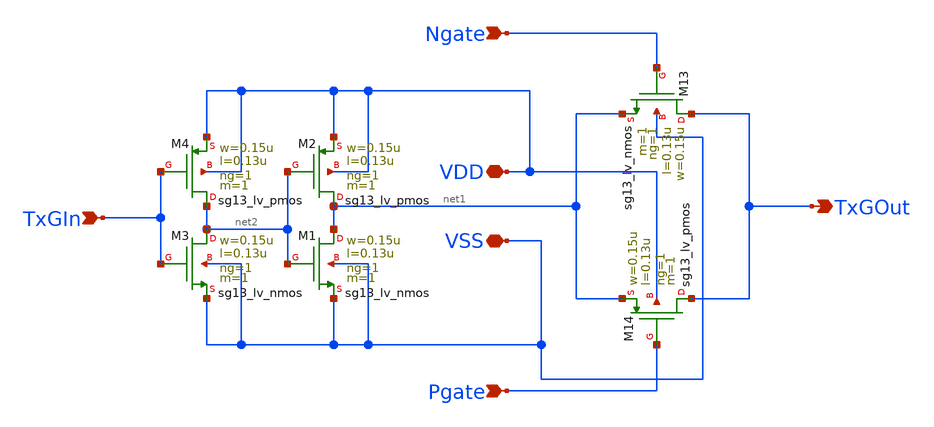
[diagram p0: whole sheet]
** sch_path: circuit_files/xschem_symbols/TxGate.sch
**.subckt TxGate Ngate Pgate TxGIn TxGOut VDD VSS
*.ipin Ngate
*.ipin Pgate
*.ipin TxGIn
*.opin TxGOut
*.iopin VDD
*.iopin VSS
XM13 TxGOut Ngate net1 VSS sg13_lv_nmos w=0.15u l=0.13u ng=1 m=1 mm_ok=1
XM14 TxGOut Pgate net1 VDD sg13_lv_pmos w=0.15u l=0.13u ng=1 m=1 mm_ok=1
XM1 net1 net2 VSS VSS sg13_lv_nmos w=0.15u l=0.13u ng=1 m=1 mm_ok=1
XM2 net1 net2 VDD VDD sg13_lv_pmos w=0.15u l=0.13u ng=1 m=1 mm_ok=1
XM3 net2 TxGIn VSS VSS sg13_lv_nmos w=0.15u l=0.13u ng=1 m=1 mm_ok=1
XM4 net2 TxGIn VDD VDD sg13_lv_pmos w=0.15u l=0.13u ng=1 m=1 mm_ok=1
**.ends
.end
